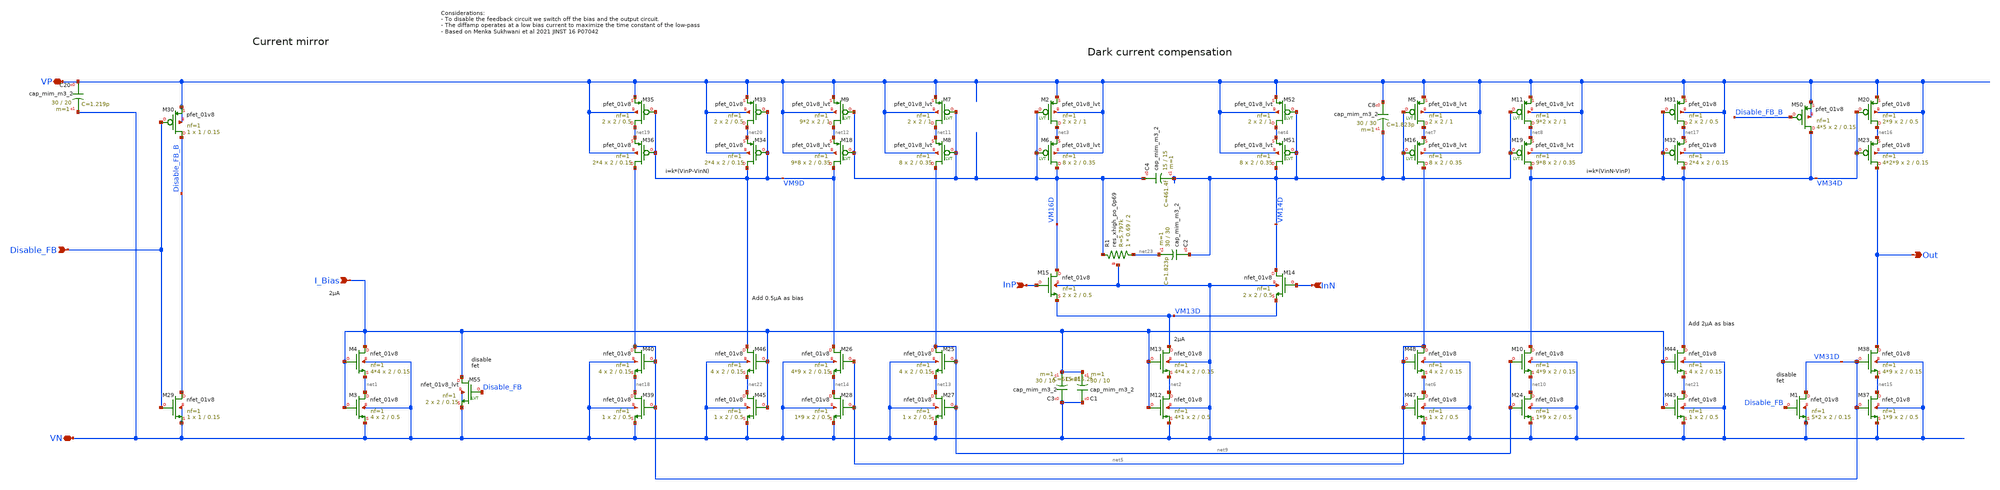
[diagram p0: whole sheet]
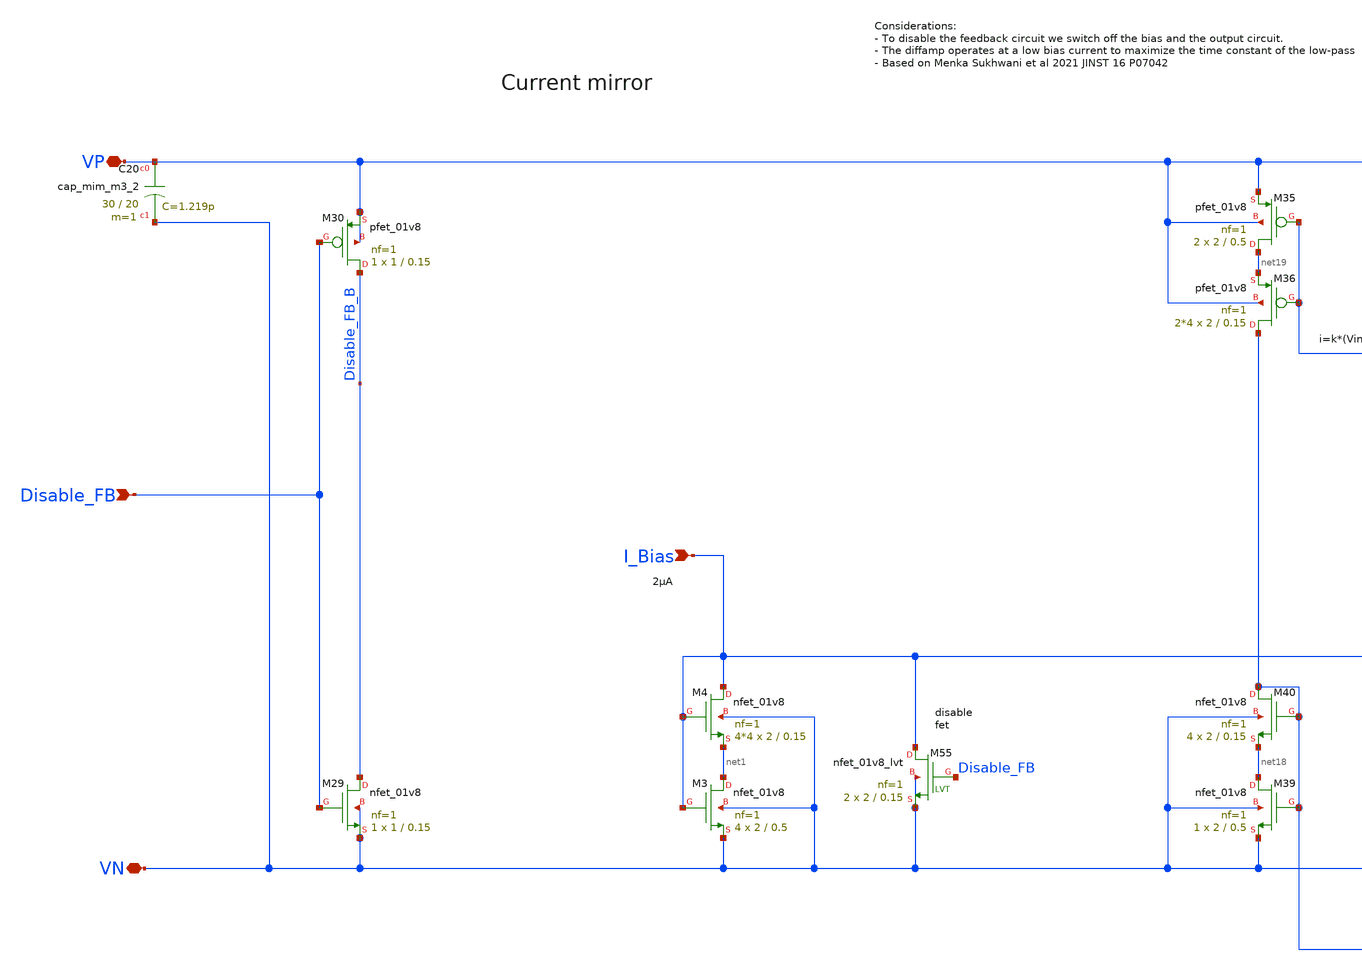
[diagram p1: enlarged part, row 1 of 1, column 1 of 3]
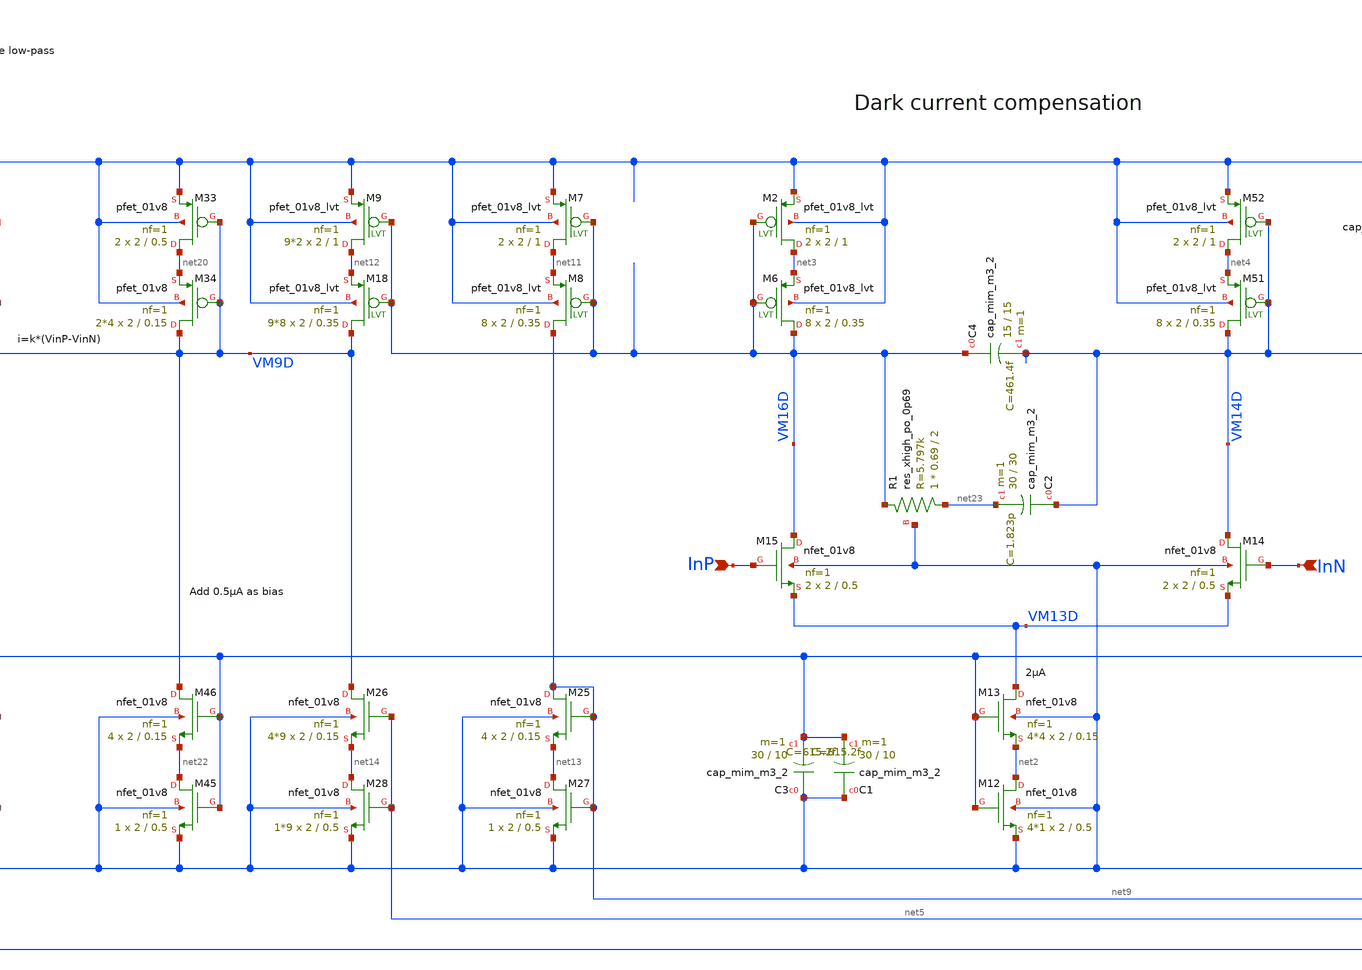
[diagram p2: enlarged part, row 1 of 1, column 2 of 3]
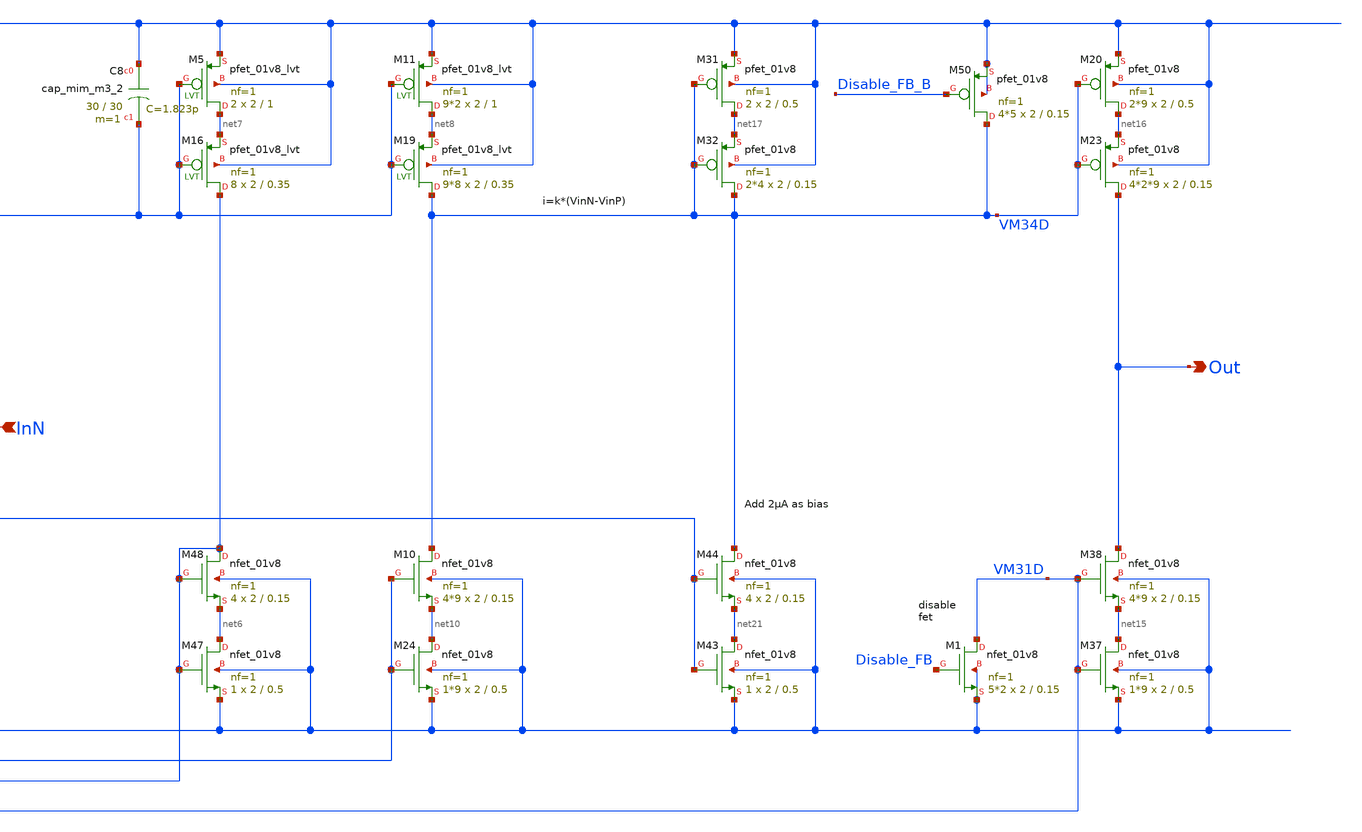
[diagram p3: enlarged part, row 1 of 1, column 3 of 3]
** sch_path: xschem/tia/feedback_sukwani.sch
**.subckt feedback_sukwani VN VP I_Bias Disable_FB InP InN Out
*.iopin VN
*.iopin VP
*.ipin I_Bias
*.ipin Disable_FB
*.ipin InP
*.ipin InN
*.opin Out
XM3 net1 I_Bias VN VN sky130_fd_pr__nfet_01v8 L=0.5 W=2 nf=1 ad='int((nf+1)/2) * W/nf * 0.29' as='int((nf+2)/2) * W/nf * 0.29'
+ pd='2*int((nf+1)/2) * (W/nf + 0.29)' ps='2*int((nf+2)/2) * (W/nf + 0.29)' nrd='0.29 / W' nrs='0.29 / W'
+ sa=0 sb=0 sd=0 mult=4 m=4
XM4 I_Bias I_Bias net1 VN sky130_fd_pr__nfet_01v8 L=0.15 W=2 nf=1 ad='int((nf+1)/2) * W/nf * 0.29' as='int((nf+2)/2) * W/nf * 0.29'
+ pd='2*int((nf+1)/2) * (W/nf + 0.29)' ps='2*int((nf+2)/2) * (W/nf + 0.29)' nrd='0.29 / W' nrs='0.29 / W'
+ sa=0 sb=0 sd=0 mult=4*4 m=4*4
XM12 net2 I_Bias VN VN sky130_fd_pr__nfet_01v8 L=0.5 W=2 nf=1 ad='int((nf+1)/2) * W/nf * 0.29' as='int((nf+2)/2) * W/nf * 0.29'
+ pd='2*int((nf+1)/2) * (W/nf + 0.29)' ps='2*int((nf+2)/2) * (W/nf + 0.29)' nrd='0.29 / W' nrs='0.29 / W'
+ sa=0 sb=0 sd=0 mult=4*1 m=4*1
XM13 VM13D I_Bias net2 VN sky130_fd_pr__nfet_01v8 L=0.15 W=2 nf=1 ad='int((nf+1)/2) * W/nf * 0.29' as='int((nf+2)/2) * W/nf * 0.29'
+ pd='2*int((nf+1)/2) * (W/nf + 0.29)' ps='2*int((nf+2)/2) * (W/nf + 0.29)' nrd='0.29 / W' nrs='0.29 / W'
+ sa=0 sb=0 sd=0 mult=4*4 m=4*4
XM29 Disable_FB_B Disable_FB VN VN sky130_fd_pr__nfet_01v8 L=0.15 W=1 nf=1 ad='int((nf+1)/2) * W/nf * 0.29'
+ as='int((nf+2)/2) * W/nf * 0.29' pd='2*int((nf+1)/2) * (W/nf + 0.29)' ps='2*int((nf+2)/2) * (W/nf + 0.29)'
+ nrd='0.29 / W' nrs='0.29 / W' sa=0 sb=0 sd=0 mult=1 m=1
XM30 Disable_FB_B Disable_FB VP VP sky130_fd_pr__pfet_01v8 L=0.15 W=1 nf=1 ad='int((nf+1)/2) * W/nf * 0.29'
+ as='int((nf+2)/2) * W/nf * 0.29' pd='2*int((nf+1)/2) * (W/nf + 0.29)' ps='2*int((nf+2)/2) * (W/nf + 0.29)'
+ nrd='0.29 / W' nrs='0.29 / W' sa=0 sb=0 sd=0 mult=1 m=1
XM47 net6 net5 VN VN sky130_fd_pr__nfet_01v8 L=0.5 W=2 nf=1 ad='int((nf+1)/2) * W/nf * 0.29' as='int((nf+2)/2) * W/nf * 0.29'
+ pd='2*int((nf+1)/2) * (W/nf + 0.29)' ps='2*int((nf+2)/2) * (W/nf + 0.29)' nrd='0.29 / W' nrs='0.29 / W'
+ sa=0 sb=0 sd=0 mult=1 m=1
XM48 net5 net5 net6 VN sky130_fd_pr__nfet_01v8 L=0.15 W=2 nf=1 ad='int((nf+1)/2) * W/nf * 0.29' as='int((nf+2)/2) * W/nf * 0.29'
+ pd='2*int((nf+1)/2) * (W/nf + 0.29)' ps='2*int((nf+2)/2) * (W/nf + 0.29)' nrd='0.29 / W' nrs='0.29 / W'
+ sa=0 sb=0 sd=0 mult=4 m=4
XC8 VP VM14D sky130_fd_pr__cap_mim_m3_2 W=30 L=30 MF=1 m=1
XC20 VP VN sky130_fd_pr__cap_mim_m3_2 W=30 L=20 MF=1 m=1
XM55 I_Bias Disable_FB VN VN sky130_fd_pr__nfet_01v8_lvt L=0.15 W=2 nf=1 ad='int((nf+1)/2) * W/nf * 0.29'
+ as='int((nf+2)/2) * W/nf * 0.29' pd='2*int((nf+1)/2) * (W/nf + 0.29)' ps='2*int((nf+2)/2) * (W/nf + 0.29)'
+ nrd='0.29 / W' nrs='0.29 / W' sa=0 sb=0 sd=0 mult=2 m=2
XM15 VM16D InP VM13D VN sky130_fd_pr__nfet_01v8 L=0.5 W=2 nf=1 ad='int((nf+1)/2) * W/nf * 0.29' as='int((nf+2)/2) * W/nf * 0.29'
+ pd='2*int((nf+1)/2) * (W/nf + 0.29)' ps='2*int((nf+2)/2) * (W/nf + 0.29)' nrd='0.29 / W' nrs='0.29 / W'
+ sa=0 sb=0 sd=0 mult=2 m=2
XM14 VM14D InN VM13D VN sky130_fd_pr__nfet_01v8 L=0.5 W=2 nf=1 ad='int((nf+1)/2) * W/nf * 0.29' as='int((nf+2)/2) * W/nf * 0.29'
+ pd='2*int((nf+1)/2) * (W/nf + 0.29)' ps='2*int((nf+2)/2) * (W/nf + 0.29)' nrd='0.29 / W' nrs='0.29 / W'
+ sa=0 sb=0 sd=0 mult=2 m=2
XM10 VM34D net9 net10 VN sky130_fd_pr__nfet_01v8 L=0.15 W=2 nf=1 ad='int((nf+1)/2) * W/nf * 0.29' as='int((nf+2)/2) * W/nf * 0.29'
+ pd='2*int((nf+1)/2) * (W/nf + 0.29)' ps='2*int((nf+2)/2) * (W/nf + 0.29)' nrd='0.29 / W' nrs='0.29 / W'
+ sa=0 sb=0 sd=0 mult=4*9 m=4*9
XM24 net10 net9 VN VN sky130_fd_pr__nfet_01v8 L=0.5 W=2 nf=1 ad='int((nf+1)/2) * W/nf * 0.29' as='int((nf+2)/2) * W/nf * 0.29'
+ pd='2*int((nf+1)/2) * (W/nf + 0.29)' ps='2*int((nf+2)/2) * (W/nf + 0.29)' nrd='0.29 / W' nrs='0.29 / W'
+ sa=0 sb=0 sd=0 mult=1*9 m=1*9
XM25 net9 net9 net13 VN sky130_fd_pr__nfet_01v8 L=0.15 W=2 nf=1 ad='int((nf+1)/2) * W/nf * 0.29' as='int((nf+2)/2) * W/nf * 0.29'
+ pd='2*int((nf+1)/2) * (W/nf + 0.29)' ps='2*int((nf+2)/2) * (W/nf + 0.29)' nrd='0.29 / W' nrs='0.29 / W'
+ sa=0 sb=0 sd=0 mult=4 m=4
XM26 VM9D net5 net14 VN sky130_fd_pr__nfet_01v8 L=0.15 W=2 nf=1 ad='int((nf+1)/2) * W/nf * 0.29' as='int((nf+2)/2) * W/nf * 0.29'
+ pd='2*int((nf+1)/2) * (W/nf + 0.29)' ps='2*int((nf+2)/2) * (W/nf + 0.29)' nrd='0.29 / W' nrs='0.29 / W'
+ sa=0 sb=0 sd=0 mult=4*9 m=4*9
XM27 net13 net9 VN VN sky130_fd_pr__nfet_01v8 L=0.5 W=2 nf=1 ad='int((nf+1)/2) * W/nf * 0.29' as='int((nf+2)/2) * W/nf * 0.29'
+ pd='2*int((nf+1)/2) * (W/nf + 0.29)' ps='2*int((nf+2)/2) * (W/nf + 0.29)' nrd='0.29 / W' nrs='0.29 / W'
+ sa=0 sb=0 sd=0 mult=1 m=1
XM28 net14 net5 VN VN sky130_fd_pr__nfet_01v8 L=0.5 W=2 nf=1 ad='int((nf+1)/2) * W/nf * 0.29' as='int((nf+2)/2) * W/nf * 0.29'
+ pd='2*int((nf+1)/2) * (W/nf + 0.29)' ps='2*int((nf+2)/2) * (W/nf + 0.29)' nrd='0.29 / W' nrs='0.29 / W'
+ sa=0 sb=0 sd=0 mult=1*9 m=1*9
XM43 net21 I_Bias VN VN sky130_fd_pr__nfet_01v8 L=0.5 W=2 nf=1 ad='int((nf+1)/2) * W/nf * 0.29' as='int((nf+2)/2) * W/nf * 0.29'
+ pd='2*int((nf+1)/2) * (W/nf + 0.29)' ps='2*int((nf+2)/2) * (W/nf + 0.29)' nrd='0.29 / W' nrs='0.29 / W'
+ sa=0 sb=0 sd=0 mult=1 m=1
XM44 VM34D I_Bias net21 VN sky130_fd_pr__nfet_01v8 L=0.15 W=2 nf=1 ad='int((nf+1)/2) * W/nf * 0.29' as='int((nf+2)/2) * W/nf * 0.29'
+ pd='2*int((nf+1)/2) * (W/nf + 0.29)' ps='2*int((nf+2)/2) * (W/nf + 0.29)' nrd='0.29 / W' nrs='0.29 / W'
+ sa=0 sb=0 sd=0 mult=4 m=4
XM45 net22 I_Bias VN VN sky130_fd_pr__nfet_01v8 L=0.5 W=2 nf=1 ad='int((nf+1)/2) * W/nf * 0.29' as='int((nf+2)/2) * W/nf * 0.29'
+ pd='2*int((nf+1)/2) * (W/nf + 0.29)' ps='2*int((nf+2)/2) * (W/nf + 0.29)' nrd='0.29 / W' nrs='0.29 / W'
+ sa=0 sb=0 sd=0 mult=1 m=1
XM46 VM9D I_Bias net22 VN sky130_fd_pr__nfet_01v8 L=0.15 W=2 nf=1 ad='int((nf+1)/2) * W/nf * 0.29' as='int((nf+2)/2) * W/nf * 0.29'
+ pd='2*int((nf+1)/2) * (W/nf + 0.29)' ps='2*int((nf+2)/2) * (W/nf + 0.29)' nrd='0.29 / W' nrs='0.29 / W'
+ sa=0 sb=0 sd=0 mult=4 m=4
XM50 VM34D Disable_FB_B VP VP sky130_fd_pr__pfet_01v8 L=0.15 W=2 nf=1 ad='int((nf+1)/2) * W/nf * 0.29'
+ as='int((nf+2)/2) * W/nf * 0.29' pd='2*int((nf+1)/2) * (W/nf + 0.29)' ps='2*int((nf+2)/2) * (W/nf + 0.29)'
+ nrd='0.29 / W' nrs='0.29 / W' sa=0 sb=0 sd=0 mult=4*5 m=4*5
XM51 VM14D VM14D net4 VP sky130_fd_pr__pfet_01v8_lvt L=0.35 W=2 nf=1 ad='int((nf+1)/2) * W/nf * 0.29'
+ as='int((nf+2)/2) * W/nf * 0.29' pd='2*int((nf+1)/2) * (W/nf + 0.29)' ps='2*int((nf+2)/2) * (W/nf + 0.29)'
+ nrd='0.29 / W' nrs='0.29 / W' sa=0 sb=0 sd=0 mult=8 m=8
XM52 net4 VM14D VP VP sky130_fd_pr__pfet_01v8_lvt L=1 W=2 nf=1 ad='int((nf+1)/2) * W/nf * 0.29' as='int((nf+2)/2) * W/nf * 0.29'
+ pd='2*int((nf+1)/2) * (W/nf + 0.29)' ps='2*int((nf+2)/2) * (W/nf + 0.29)' nrd='0.29 / W' nrs='0.29 / W'
+ sa=0 sb=0 sd=0 mult=2 m=2
XM5 net7 VM14D VP VP sky130_fd_pr__pfet_01v8_lvt L=1 W=2 nf=1 ad='int((nf+1)/2) * W/nf * 0.29' as='int((nf+2)/2) * W/nf * 0.29'
+ pd='2*int((nf+1)/2) * (W/nf + 0.29)' ps='2*int((nf+2)/2) * (W/nf + 0.29)' nrd='0.29 / W' nrs='0.29 / W'
+ sa=0 sb=0 sd=0 mult=2 m=2
XM11 net8 VM14D VP VP sky130_fd_pr__pfet_01v8_lvt L=1 W=2 nf=1 ad='int((nf+1)/2) * W/nf * 0.29' as='int((nf+2)/2) * W/nf * 0.29'
+ pd='2*int((nf+1)/2) * (W/nf + 0.29)' ps='2*int((nf+2)/2) * (W/nf + 0.29)' nrd='0.29 / W' nrs='0.29 / W'
+ sa=0 sb=0 sd=0 mult=9*2 m=9*2
XM16 net5 VM14D net7 VP sky130_fd_pr__pfet_01v8_lvt L=0.35 W=2 nf=1 ad='int((nf+1)/2) * W/nf * 0.29'
+ as='int((nf+2)/2) * W/nf * 0.29' pd='2*int((nf+1)/2) * (W/nf + 0.29)' ps='2*int((nf+2)/2) * (W/nf + 0.29)'
+ nrd='0.29 / W' nrs='0.29 / W' sa=0 sb=0 sd=0 mult=8 m=8
XM19 VM34D VM14D net8 VP sky130_fd_pr__pfet_01v8_lvt L=0.35 W=2 nf=1 ad='int((nf+1)/2) * W/nf * 0.29'
+ as='int((nf+2)/2) * W/nf * 0.29' pd='2*int((nf+1)/2) * (W/nf + 0.29)' ps='2*int((nf+2)/2) * (W/nf + 0.29)'
+ nrd='0.29 / W' nrs='0.29 / W' sa=0 sb=0 sd=0 mult=9*8 m=9*8
XM2 net3 VM16D VP VP sky130_fd_pr__pfet_01v8_lvt L=1 W=2 nf=1 ad='int((nf+1)/2) * W/nf * 0.29' as='int((nf+2)/2) * W/nf * 0.29'
+ pd='2*int((nf+1)/2) * (W/nf + 0.29)' ps='2*int((nf+2)/2) * (W/nf + 0.29)' nrd='0.29 / W' nrs='0.29 / W'
+ sa=0 sb=0 sd=0 mult=2 m=2
XM6 VM16D VM16D net3 VP sky130_fd_pr__pfet_01v8_lvt L=0.35 W=2 nf=1 ad='int((nf+1)/2) * W/nf * 0.29'
+ as='int((nf+2)/2) * W/nf * 0.29' pd='2*int((nf+1)/2) * (W/nf + 0.29)' ps='2*int((nf+2)/2) * (W/nf + 0.29)'
+ nrd='0.29 / W' nrs='0.29 / W' sa=0 sb=0 sd=0 mult=8 m=8
XM7 net11 VM16D VP VP sky130_fd_pr__pfet_01v8_lvt L=1 W=2 nf=1 ad='int((nf+1)/2) * W/nf * 0.29' as='int((nf+2)/2) * W/nf * 0.29'
+ pd='2*int((nf+1)/2) * (W/nf + 0.29)' ps='2*int((nf+2)/2) * (W/nf + 0.29)' nrd='0.29 / W' nrs='0.29 / W'
+ sa=0 sb=0 sd=0 mult=2 m=2
XM8 net9 VM16D net11 VP sky130_fd_pr__pfet_01v8_lvt L=0.35 W=2 nf=1 ad='int((nf+1)/2) * W/nf * 0.29'
+ as='int((nf+2)/2) * W/nf * 0.29' pd='2*int((nf+1)/2) * (W/nf + 0.29)' ps='2*int((nf+2)/2) * (W/nf + 0.29)'
+ nrd='0.29 / W' nrs='0.29 / W' sa=0 sb=0 sd=0 mult=8 m=8
XM9 net12 VM16D VP VP sky130_fd_pr__pfet_01v8_lvt L=1 W=2 nf=1 ad='int((nf+1)/2) * W/nf * 0.29' as='int((nf+2)/2) * W/nf * 0.29'
+ pd='2*int((nf+1)/2) * (W/nf + 0.29)' ps='2*int((nf+2)/2) * (W/nf + 0.29)' nrd='0.29 / W' nrs='0.29 / W'
+ sa=0 sb=0 sd=0 mult=9*2 m=9*2
XM18 VM9D VM16D net12 VP sky130_fd_pr__pfet_01v8_lvt L=0.35 W=2 nf=1 ad='int((nf+1)/2) * W/nf * 0.29'
+ as='int((nf+2)/2) * W/nf * 0.29' pd='2*int((nf+1)/2) * (W/nf + 0.29)' ps='2*int((nf+2)/2) * (W/nf + 0.29)'
+ nrd='0.29 / W' nrs='0.29 / W' sa=0 sb=0 sd=0 mult=9*8 m=9*8
XM20 net16 VM34D VP VP sky130_fd_pr__pfet_01v8 L=0.5 W=2 nf=1 ad='int((nf+1)/2) * W/nf * 0.29' as='int((nf+2)/2) * W/nf * 0.29'
+ pd='2*int((nf+1)/2) * (W/nf + 0.29)' ps='2*int((nf+2)/2) * (W/nf + 0.29)' nrd='0.29 / W' nrs='0.29 / W'
+ sa=0 sb=0 sd=0 mult=2*9 m=2*9
XC3 VN I_Bias sky130_fd_pr__cap_mim_m3_2 W=30 L=10 MF=1 m=1
XM23 Out VM34D net16 VP sky130_fd_pr__pfet_01v8 L=0.15 W=2 nf=1 ad='int((nf+1)/2) * W/nf * 0.29' as='int((nf+2)/2) * W/nf * 0.29'
+ pd='2*int((nf+1)/2) * (W/nf + 0.29)' ps='2*int((nf+2)/2) * (W/nf + 0.29)' nrd='0.29 / W' nrs='0.29 / W'
+ sa=0 sb=0 sd=0 mult=4*2*9 m=4*2*9
XM31 net17 VM34D VP VP sky130_fd_pr__pfet_01v8 L=0.5 W=2 nf=1 ad='int((nf+1)/2) * W/nf * 0.29' as='int((nf+2)/2) * W/nf * 0.29'
+ pd='2*int((nf+1)/2) * (W/nf + 0.29)' ps='2*int((nf+2)/2) * (W/nf + 0.29)' nrd='0.29 / W' nrs='0.29 / W'
+ sa=0 sb=0 sd=0 mult=2 m=2
XM32 VM34D VM34D net17 VP sky130_fd_pr__pfet_01v8 L=0.15 W=2 nf=1 ad='int((nf+1)/2) * W/nf * 0.29' as='int((nf+2)/2) * W/nf * 0.29'
+ pd='2*int((nf+1)/2) * (W/nf + 0.29)' ps='2*int((nf+2)/2) * (W/nf + 0.29)' nrd='0.29 / W' nrs='0.29 / W'
+ sa=0 sb=0 sd=0 mult=2*4 m=2*4
XM33 net20 VM9D VP VP sky130_fd_pr__pfet_01v8 L=0.5 W=2 nf=1 ad='int((nf+1)/2) * W/nf * 0.29' as='int((nf+2)/2) * W/nf * 0.29'
+ pd='2*int((nf+1)/2) * (W/nf + 0.29)' ps='2*int((nf+2)/2) * (W/nf + 0.29)' nrd='0.29 / W' nrs='0.29 / W'
+ sa=0 sb=0 sd=0 mult=2 m=2
XM34 VM9D VM9D net20 VP sky130_fd_pr__pfet_01v8 L=0.15 W=2 nf=1 ad='int((nf+1)/2) * W/nf * 0.29' as='int((nf+2)/2) * W/nf * 0.29'
+ pd='2*int((nf+1)/2) * (W/nf + 0.29)' ps='2*int((nf+2)/2) * (W/nf + 0.29)' nrd='0.29 / W' nrs='0.29 / W'
+ sa=0 sb=0 sd=0 mult=2*4 m=2*4
XM35 net19 VM9D VP VP sky130_fd_pr__pfet_01v8 L=0.5 W=2 nf=1 ad='int((nf+1)/2) * W/nf * 0.29' as='int((nf+2)/2) * W/nf * 0.29'
+ pd='2*int((nf+1)/2) * (W/nf + 0.29)' ps='2*int((nf+2)/2) * (W/nf + 0.29)' nrd='0.29 / W' nrs='0.29 / W'
+ sa=0 sb=0 sd=0 mult=2 m=2
XM36 VM31D VM9D net19 VP sky130_fd_pr__pfet_01v8 L=0.15 W=2 nf=1 ad='int((nf+1)/2) * W/nf * 0.29' as='int((nf+2)/2) * W/nf * 0.29'
+ pd='2*int((nf+1)/2) * (W/nf + 0.29)' ps='2*int((nf+2)/2) * (W/nf + 0.29)' nrd='0.29 / W' nrs='0.29 / W'
+ sa=0 sb=0 sd=0 mult=2*4 m=2*4
XM37 net15 VM31D VN VN sky130_fd_pr__nfet_01v8 L=0.5 W=2 nf=1 ad='int((nf+1)/2) * W/nf * 0.29' as='int((nf+2)/2) * W/nf * 0.29'
+ pd='2*int((nf+1)/2) * (W/nf + 0.29)' ps='2*int((nf+2)/2) * (W/nf + 0.29)' nrd='0.29 / W' nrs='0.29 / W'
+ sa=0 sb=0 sd=0 mult=1*9 m=1*9
XM38 Out VM31D net15 VN sky130_fd_pr__nfet_01v8 L=0.15 W=2 nf=1 ad='int((nf+1)/2) * W/nf * 0.29' as='int((nf+2)/2) * W/nf * 0.29'
+ pd='2*int((nf+1)/2) * (W/nf + 0.29)' ps='2*int((nf+2)/2) * (W/nf + 0.29)' nrd='0.29 / W' nrs='0.29 / W'
+ sa=0 sb=0 sd=0 mult=4*9 m=4*9
XM39 net18 VM31D VN VN sky130_fd_pr__nfet_01v8 L=0.5 W=2 nf=1 ad='int((nf+1)/2) * W/nf * 0.29' as='int((nf+2)/2) * W/nf * 0.29'
+ pd='2*int((nf+1)/2) * (W/nf + 0.29)' ps='2*int((nf+2)/2) * (W/nf + 0.29)' nrd='0.29 / W' nrs='0.29 / W'
+ sa=0 sb=0 sd=0 mult=1 m=1
XM40 VM31D VM31D net18 VN sky130_fd_pr__nfet_01v8 L=0.15 W=2 nf=1 ad='int((nf+1)/2) * W/nf * 0.29' as='int((nf+2)/2) * W/nf * 0.29'
+ pd='2*int((nf+1)/2) * (W/nf + 0.29)' ps='2*int((nf+2)/2) * (W/nf + 0.29)' nrd='0.29 / W' nrs='0.29 / W'
+ sa=0 sb=0 sd=0 mult=4 m=4
XM1 VM31D Disable_FB VN VN sky130_fd_pr__nfet_01v8 L=0.15 W=2 nf=1 ad='int((nf+1)/2) * W/nf * 0.29' as='int((nf+2)/2) * W/nf * 0.29'
+ pd='2*int((nf+1)/2) * (W/nf + 0.29)' ps='2*int((nf+2)/2) * (W/nf + 0.29)' nrd='0.29 / W' nrs='0.29 / W'
+ sa=0 sb=0 sd=0 mult=5*2 m=5*2
XC1 VN I_Bias sky130_fd_pr__cap_mim_m3_2 W=30 L=10 MF=1 m=1
XC4 VM16D VM14D sky130_fd_pr__cap_mim_m3_2 W=15 L=15 MF=1 m=1
XC2 VM14D net23 sky130_fd_pr__cap_mim_m3_2 W=30 L=30 MF=1 m=1
XR1 net23 VM16D VN sky130_fd_pr__res_xhigh_po_0p69 L=2 mult=1 m=1
**.ends
.end
